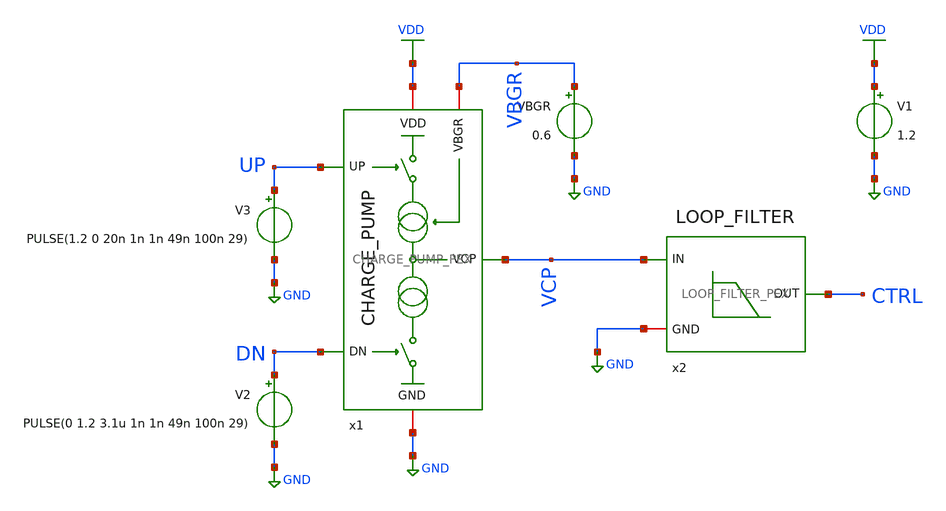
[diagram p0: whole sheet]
** sch_path: xschem/charge-pump/tb_CP_LF_PEX.sch
**.subckt tb_CP_LF_PEX
V1 VDD GND 1.2
V2 DN GND PULSE(0 1.2 3.1u 1n 1n 49n 100n 29)
V3 UP GND PULSE(1.2 0 20n 1n 1n 49n 100n 29)
VBGR VBGR GND 0.6
x1 UP VDD VCP VBGR GND DN CHARGE_PUMP_PEX
x2 CTRL VCP GND LOOP_FILTER_PEX
**** begin user architecture code



.include tb_CP.save
.param temp=27
.option method=gear rshunt=1.0e12
.control
save all
op
write tb_CP_LF.raw
.endc




.include /foss/designs/unicasss-tools/SG13G2_2.4GHz_LC_VCO_FPLL/pex/CHARGE_PUMP_V2__CHARGE_PUMP/magic_RC/CHARGE_PUMP.pex.spice
.include /foss/designs/unicasss-tools/SG13G2_2.4GHz_LC_VCO_FPLL/pex/LOOP_FILTER__LOOP_FILTER/magic_RC/LOOP_FILTER.pex.spice
.lib cornerMOSlv.lib mos_tt
.lib cornerMOShv.lib mos_tt
.lib cornerRES.lib res_typ
.lib cornerCAP.lib cap_typ




.param temp = 27
.options method=gear rshunt=1.0e12

.control

* Save required signals
save v(UP) v(DN) v(VCP) v(CTRL)

* Long transient simulation
tran 1n 6u

* Measurements
meas tran ctrl_end find v(CTRL) at=6u
meas tran ctrl_max max v(CTRL)
meas tran ctrl_min min v(CTRL)
meas tran vcp_end find v(VCP) at=6u
meas tran vcp_max max v(VCP)
* supply current (negative = drawn from the source), power = 1.2 V x |idd|
meas tran idd avg i(V1) from=1u to=6u

write tb_CP_LF_PEX_tran.raw v(UP) v(DN) v(VCP) v(CTRL)

* Plot transient waveform
plot v(UP) v(DN) v(VCP) v(CTRL)
plot v(CTRL)

.endc



**** end user architecture code
**.ends
.GLOBAL VDD
.GLOBAL GND
.end
